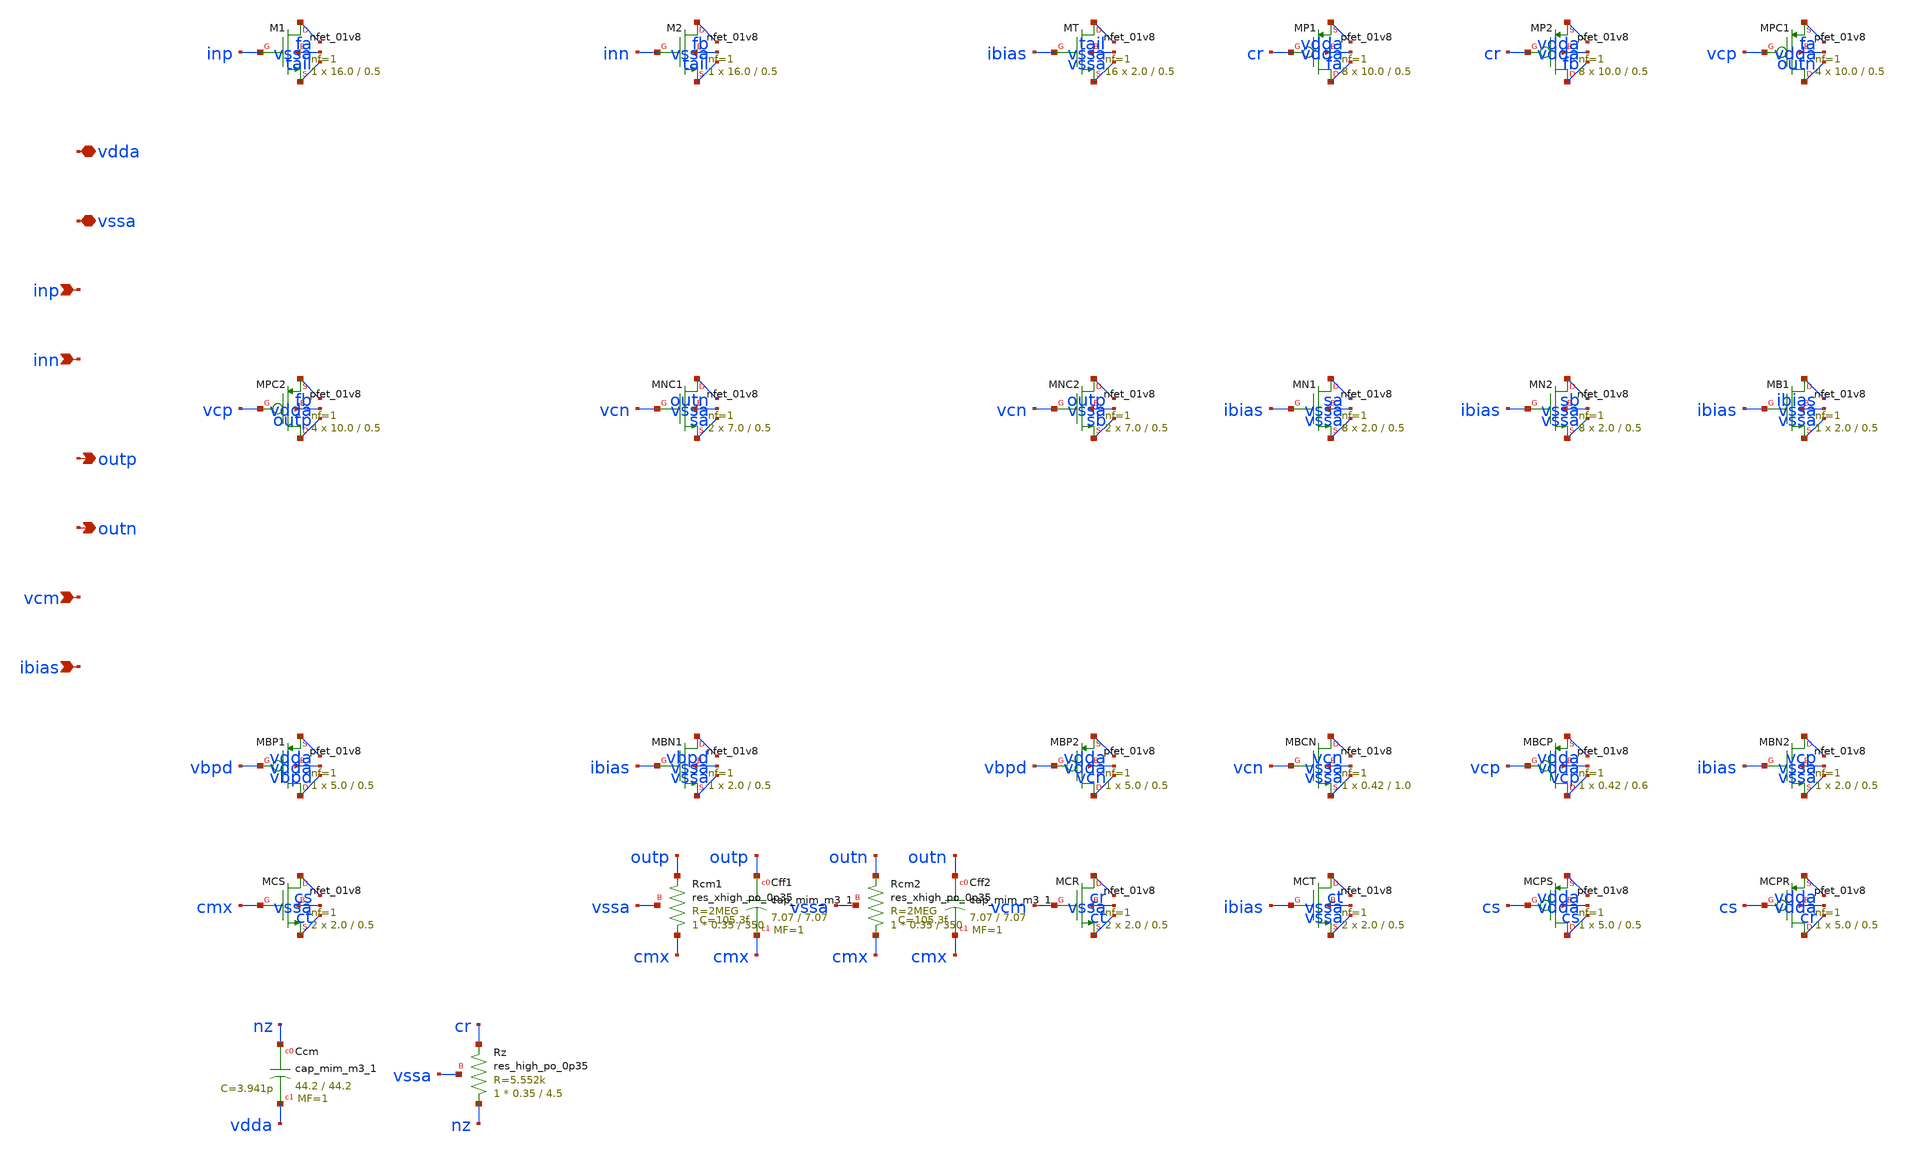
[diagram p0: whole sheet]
** sch_path: design/ota/ota_fd.sch
**.subckt ota_fd vdda vssa inp inn outp outn vcm ibias
*.iopin vdda
*.iopin vssa
*.ipin inp
*.ipin inn
*.opin outp
*.opin outn
*.ipin vcm
*.ipin ibias
XM1 fa inp tail vssa sky130_fd_pr__nfet_01v8 L=0.5 W=16.0 nf=1 ad='int((1 + 1)/2) * 16.0 / 1 * 0.29'
+ as='int((1 + 2)/2) * 16.0 / 1 * 0.29' pd='2*int((1 + 1)/2) * (16.0 / 1 + 0.29)' ps='2*int((1 + 2)/2) * (16.0 / 1 + 0.29)'
+ nrd='0.29 / 16.0 ' nrs='0.29 / 16.0 ' sa=0 sb=0 sd=0 mult=1 m=1
XM2 fb inn tail vssa sky130_fd_pr__nfet_01v8 L=0.5 W=16.0 nf=1 ad='int((1 + 1)/2) * 16.0 / 1 * 0.29'
+ as='int((1 + 2)/2) * 16.0 / 1 * 0.29' pd='2*int((1 + 1)/2) * (16.0 / 1 + 0.29)' ps='2*int((1 + 2)/2) * (16.0 / 1 + 0.29)'
+ nrd='0.29 / 16.0 ' nrs='0.29 / 16.0 ' sa=0 sb=0 sd=0 mult=1 m=1
XMT tail ibias vssa vssa sky130_fd_pr__nfet_01v8 L=0.5 W=2.0 nf=1 ad='int((1 + 1)/2) * 2.0 / 1 * 0.29'
+ as='int((1 + 2)/2) * 2.0 / 1 * 0.29' pd='2*int((1 + 1)/2) * (2.0 / 1 + 0.29)' ps='2*int((1 + 2)/2) * (2.0 / 1 + 0.29)'
+ nrd='0.29 / 2.0 ' nrs='0.29 / 2.0 ' sa=0 sb=0 sd=0 mult=16 m=16
XMP1 fa cr vdda vdda sky130_fd_pr__pfet_01v8 L=0.5 W=10.0 nf=1 ad='int((nf+1)/2) * W/nf * 0.29' as='int((nf+2)/2) * W/nf * 0.29'
+ pd='2*int((nf+1)/2) * (W/nf + 0.29)' ps='2*int((nf+2)/2) * (W/nf + 0.29)' nrd='0.29 / W' nrs='0.29 / W'
+ sa=0 sb=0 sd=0 mult=8 m=8
XMP2 fb cr vdda vdda sky130_fd_pr__pfet_01v8 L=0.5 W=10.0 nf=1 ad='int((nf+1)/2) * W/nf * 0.29' as='int((nf+2)/2) * W/nf * 0.29'
+ pd='2*int((nf+1)/2) * (W/nf + 0.29)' ps='2*int((nf+2)/2) * (W/nf + 0.29)' nrd='0.29 / W' nrs='0.29 / W'
+ sa=0 sb=0 sd=0 mult=8 m=8
XMPC1 outn vcp fa vdda sky130_fd_pr__pfet_01v8 L=0.5 W=10.0 nf=1 ad='int((nf+1)/2) * W/nf * 0.29' as='int((nf+2)/2) * W/nf * 0.29'
+ pd='2*int((nf+1)/2) * (W/nf + 0.29)' ps='2*int((nf+2)/2) * (W/nf + 0.29)' nrd='0.29 / W' nrs='0.29 / W'
+ sa=0 sb=0 sd=0 mult=4 m=4
XMPC2 outp vcp fb vdda sky130_fd_pr__pfet_01v8 L=0.5 W=10.0 nf=1 ad='int((nf+1)/2) * W/nf * 0.29' as='int((nf+2)/2) * W/nf * 0.29'
+ pd='2*int((nf+1)/2) * (W/nf + 0.29)' ps='2*int((nf+2)/2) * (W/nf + 0.29)' nrd='0.29 / W' nrs='0.29 / W'
+ sa=0 sb=0 sd=0 mult=4 m=4
XMNC1 outn vcn sa vssa sky130_fd_pr__nfet_01v8 L=0.5 W=7.0 nf=1 ad='int((1 + 1)/2) * 7.0 / 1 * 0.29'
+ as='int((1 + 2)/2) * 7.0 / 1 * 0.29' pd='2*int((1 + 1)/2) * (7.0 / 1 + 0.29)' ps='2*int((1 + 2)/2) * (7.0 / 1 + 0.29)'
+ nrd='0.29 / 7.0 ' nrs='0.29 / 7.0 ' sa=0 sb=0 sd=0 mult=2 m=2
XMNC2 outp vcn sb vssa sky130_fd_pr__nfet_01v8 L=0.5 W=7.0 nf=1 ad='int((1 + 1)/2) * 7.0 / 1 * 0.29'
+ as='int((1 + 2)/2) * 7.0 / 1 * 0.29' pd='2*int((1 + 1)/2) * (7.0 / 1 + 0.29)' ps='2*int((1 + 2)/2) * (7.0 / 1 + 0.29)'
+ nrd='0.29 / 7.0 ' nrs='0.29 / 7.0 ' sa=0 sb=0 sd=0 mult=2 m=2
XMN1 sa ibias vssa vssa sky130_fd_pr__nfet_01v8 L=0.5 W=2.0 nf=1 ad='int((1 + 1)/2) * 2.0 / 1 * 0.29'
+ as='int((1 + 2)/2) * 2.0 / 1 * 0.29' pd='2*int((1 + 1)/2) * (2.0 / 1 + 0.29)' ps='2*int((1 + 2)/2) * (2.0 / 1 + 0.29)'
+ nrd='0.29 / 2.0 ' nrs='0.29 / 2.0 ' sa=0 sb=0 sd=0 mult=8 m=8
XMN2 sb ibias vssa vssa sky130_fd_pr__nfet_01v8 L=0.5 W=2.0 nf=1 ad='int((1 + 1)/2) * 2.0 / 1 * 0.29'
+ as='int((1 + 2)/2) * 2.0 / 1 * 0.29' pd='2*int((1 + 1)/2) * (2.0 / 1 + 0.29)' ps='2*int((1 + 2)/2) * (2.0 / 1 + 0.29)'
+ nrd='0.29 / 2.0 ' nrs='0.29 / 2.0 ' sa=0 sb=0 sd=0 mult=8 m=8
XMB1 ibias ibias vssa vssa sky130_fd_pr__nfet_01v8 L=0.5 W=2.0 nf=1 ad='int((1 + 1)/2) * 2.0 / 1 * 0.29'
+ as='int((1 + 2)/2) * 2.0 / 1 * 0.29' pd='2*int((1 + 1)/2) * (2.0 / 1 + 0.29)' ps='2*int((1 + 2)/2) * (2.0 / 1 + 0.29)'
+ nrd='0.29 / 2.0 ' nrs='0.29 / 2.0 ' sa=0 sb=0 sd=0 mult=1 m=1
XMBP1 vbpd vbpd vdda vdda sky130_fd_pr__pfet_01v8 L=0.5 W=5.0 nf=1 ad='int((nf+1)/2) * W/nf * 0.29' as='int((nf+2)/2) * W/nf * 0.29'
+ pd='2*int((nf+1)/2) * (W/nf + 0.29)' ps='2*int((nf+2)/2) * (W/nf + 0.29)' nrd='0.29 / W' nrs='0.29 / W'
+ sa=0 sb=0 sd=0 mult=1 m=1
XMBN1 vbpd ibias vssa vssa sky130_fd_pr__nfet_01v8 L=0.5 W=2.0 nf=1 ad='int((1 + 1)/2) * 2.0 / 1 * 0.29'
+ as='int((1 + 2)/2) * 2.0 / 1 * 0.29' pd='2*int((1 + 1)/2) * (2.0 / 1 + 0.29)' ps='2*int((1 + 2)/2) * (2.0 / 1 + 0.29)'
+ nrd='0.29 / 2.0 ' nrs='0.29 / 2.0 ' sa=0 sb=0 sd=0 mult=1 m=1
XMBP2 vcn vbpd vdda vdda sky130_fd_pr__pfet_01v8 L=0.5 W=5.0 nf=1 ad='int((nf+1)/2) * W/nf * 0.29' as='int((nf+2)/2) * W/nf * 0.29'
+ pd='2*int((nf+1)/2) * (W/nf + 0.29)' ps='2*int((nf+2)/2) * (W/nf + 0.29)' nrd='0.29 / W' nrs='0.29 / W'
+ sa=0 sb=0 sd=0 mult=1 m=1
XMBCN vcn vcn vssa vssa sky130_fd_pr__nfet_01v8 L=1.0 W=0.42 nf=1 ad='int((1 + 1)/2) * 0.42 / 1 * 0.29'
+ as='int((1 + 2)/2) * 0.42 / 1 * 0.29' pd='2*int((1 + 1)/2) * (0.42 / 1 + 0.29)' ps='2*int((1 + 2)/2) * (0.42 / 1 + 0.29)'
+ nrd='0.29 / 0.42 ' nrs='0.29 / 0.42 ' sa=0 sb=0 sd=0 mult=1 m=1
XMBCP vcp vcp vdda vdda sky130_fd_pr__pfet_01v8 L=0.6 W=0.42 nf=1 ad='int((nf+1)/2) * W/nf * 0.29' as='int((nf+2)/2) * W/nf * 0.29'
+ pd='2*int((nf+1)/2) * (W/nf + 0.29)' ps='2*int((nf+2)/2) * (W/nf + 0.29)' nrd='0.29 / W' nrs='0.29 / W'
+ sa=0 sb=0 sd=0 mult=1 m=1
XMBN2 vcp ibias vssa vssa sky130_fd_pr__nfet_01v8 L=0.5 W=2.0 nf=1 ad='int((1 + 1)/2) * 2.0 / 1 * 0.29'
+ as='int((1 + 2)/2) * 2.0 / 1 * 0.29' pd='2*int((1 + 1)/2) * (2.0 / 1 + 0.29)' ps='2*int((1 + 2)/2) * (2.0 / 1 + 0.29)'
+ nrd='0.29 / 2.0 ' nrs='0.29 / 2.0 ' sa=0 sb=0 sd=0 mult=1 m=1
XMCS cs cmx ct vssa sky130_fd_pr__nfet_01v8 L=0.5 W=2.0 nf=1 ad='int((1 + 1)/2) * 2.0 / 1 * 0.29' as='int((1 + 2)/2) * 2.0 / 1 * 0.29'
+ pd='2*int((1 + 1)/2) * (2.0 / 1 + 0.29)' ps='2*int((1 + 2)/2) * (2.0 / 1 + 0.29)' nrd='0.29 / 2.0 ' nrs='0.29 / 2.0 '
+ sa=0 sb=0 sd=0 mult=2 m=2
XRcm1 cmx outp vssa sky130_fd_pr__res_xhigh_po_0p35 L=350 mult=1 m=1
XRcm2 cmx outn vssa sky130_fd_pr__res_xhigh_po_0p35 L=350 mult=1 m=1
XCff1 outp cmx sky130_fd_pr__cap_mim_m3_1 W=7.07 L=7.07 MF=1 m=1
XCff2 outn cmx sky130_fd_pr__cap_mim_m3_1 W=7.07 L=7.07 MF=1 m=1
XMCR cr vcm ct vssa sky130_fd_pr__nfet_01v8 L=0.5 W=2.0 nf=1 ad='int((1 + 1)/2) * 2.0 / 1 * 0.29' as='int((1 + 2)/2) * 2.0 / 1 * 0.29'
+ pd='2*int((1 + 1)/2) * (2.0 / 1 + 0.29)' ps='2*int((1 + 2)/2) * (2.0 / 1 + 0.29)' nrd='0.29 / 2.0 ' nrs='0.29 / 2.0 '
+ sa=0 sb=0 sd=0 mult=2 m=2
XMCT ct ibias vssa vssa sky130_fd_pr__nfet_01v8 L=0.5 W=2.0 nf=1 ad='int((1 + 1)/2) * 2.0 / 1 * 0.29'
+ as='int((1 + 2)/2) * 2.0 / 1 * 0.29' pd='2*int((1 + 1)/2) * (2.0 / 1 + 0.29)' ps='2*int((1 + 2)/2) * (2.0 / 1 + 0.29)'
+ nrd='0.29 / 2.0 ' nrs='0.29 / 2.0 ' sa=0 sb=0 sd=0 mult=2 m=2
XMCPS cs cs vdda vdda sky130_fd_pr__pfet_01v8 L=0.5 W=5.0 nf=1 ad='int((nf+1)/2) * W/nf * 0.29' as='int((nf+2)/2) * W/nf * 0.29'
+ pd='2*int((nf+1)/2) * (W/nf + 0.29)' ps='2*int((nf+2)/2) * (W/nf + 0.29)' nrd='0.29 / W' nrs='0.29 / W'
+ sa=0 sb=0 sd=0 mult=1 m=1
XMCPR cr cs vdda vdda sky130_fd_pr__pfet_01v8 L=0.5 W=5.0 nf=1 ad='int((nf+1)/2) * W/nf * 0.29' as='int((nf+2)/2) * W/nf * 0.29'
+ pd='2*int((nf+1)/2) * (W/nf + 0.29)' ps='2*int((nf+2)/2) * (W/nf + 0.29)' nrd='0.29 / W' nrs='0.29 / W'
+ sa=0 sb=0 sd=0 mult=1 m=1
XCcm nz vdda sky130_fd_pr__cap_mim_m3_1 W=44.2 L=44.2 MF=1 m=1
XRz nz cr vssa sky130_fd_pr__res_high_po_0p35 L=4.5 mult=1 m=1
**.ends
.end
